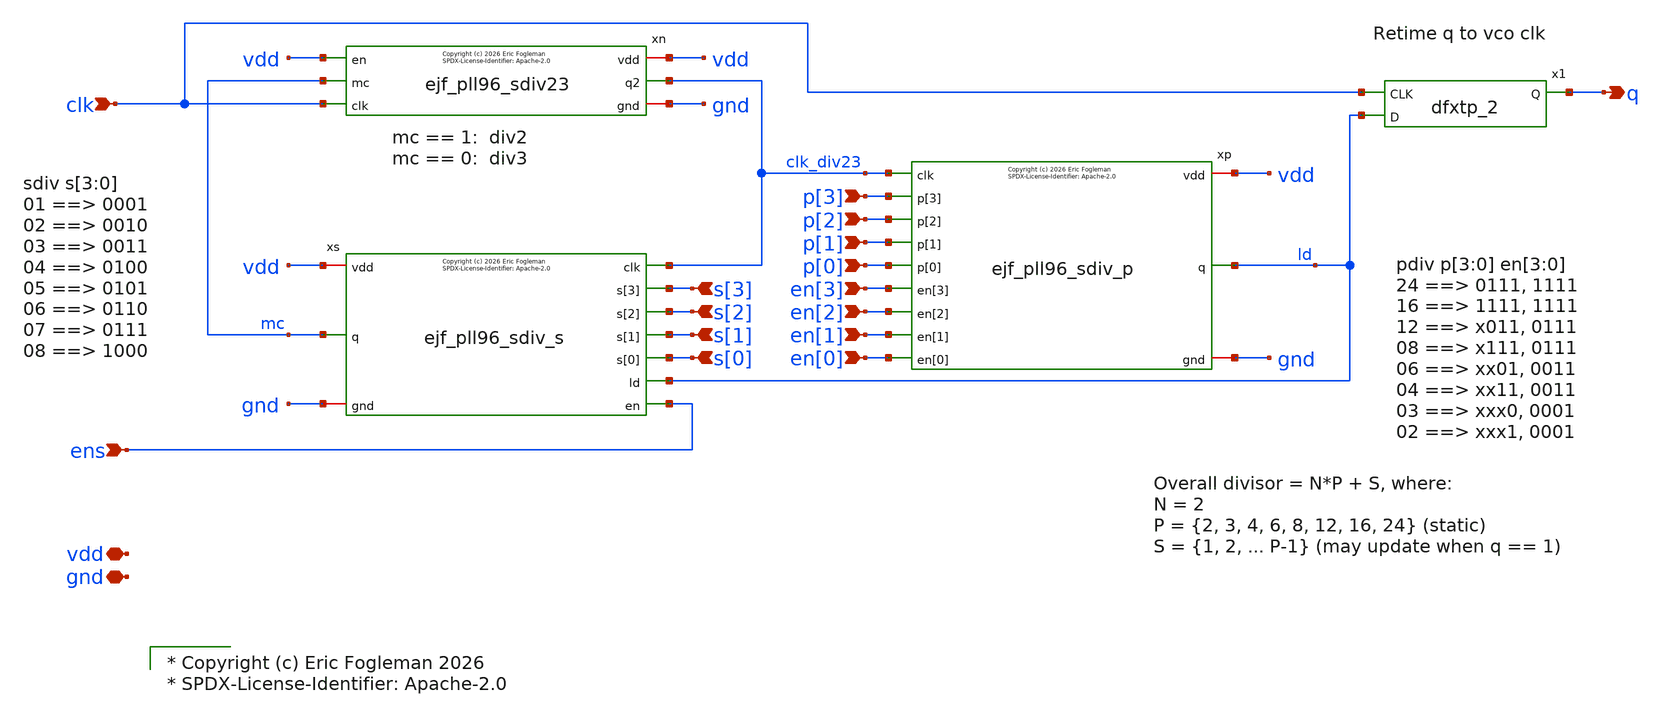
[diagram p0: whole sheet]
** sch_path: xschem/ejf_pll96_sdiv_mm.sch
* xschem/ejf_pll96_sdiv23.sym:
* Copyright (c) 2026 Eric Fogleman

* Copyright (c) Eric Fogleman 2026
* SPDX-License-Identifier: Apache-2.0

**.subckt ejf_pll96_sdiv_mm gnd clk q vdd p[3] p[2] p[1] p[0] en[3] en[2] en[1] s[0] s[1] s[2] s[3]
*+ ens en[0]
*.iopin gnd
*.ipin clk
*.opin q
*.iopin vdd
*.ipin p[3]
*.ipin p[2]
*.ipin p[1]
*.ipin p[0]
*.ipin en[3]
*.ipin en[2]
*.ipin en[1]
*.ipin s[0]
*.ipin s[1]
*.ipin s[2]
*.ipin s[3]
*.ipin ens
*.ipin en[0]
xn clk_div23 clk mc vdd gnd vdd ejf_pll96_sdiv23
xp clk_div23 p[0] en[1] p[1] ld en[2] p[2] en[3] p[3] vdd gnd en[0] ejf_pll96_sdiv_p
xs clk_div23 s[0] s[1] s[3] s[2] ld mc vdd gnd ens ejf_pll96_sdiv_s
x1 clk ld gnd gnd vdd vdd q sky130_fd_sc_ls__dfxtp_2
**.ends

* expanding   symbol:  ejf_pll96_sdiv23.sym # of pins=6
** sym_path: xschem/ejf_pll96_sdiv23.sym
** sch_path: xschem/ejf_pll96_sdiv23.sch
.subckt ejf_pll96_sdiv23 q2 clk mc vdd gnd en
*.ipin clk
*.ipin mc
*.opin q2
*.iopin vdd
*.iopin gnd
*.ipin en
x3 q1 mc q2_b gnd gnd vdd vdd d2 sky130_fd_sc_ls__o21a_1
**** begin user architecture code

* Copyright (c) Eric Fogleman 2026
* SPDX-License-Identifier: Apache-2.0

**** end user architecture code
x1 clk q2_b en gnd gnd vdd vdd q1 sky130_fd_sc_ls__edfxtp_1
x2 clk d2 en gnd gnd vdd vdd q2 q2_b sky130_fd_sc_ls__edfxbp_1
.ends


* expanding   symbol:  ejf_pll96_sdiv_p.sym # of pins=12
** sym_path: xschem/ejf_pll96_sdiv_p.sym
** sch_path: xschem/ejf_pll96_sdiv_p.sch
.subckt ejf_pll96_sdiv_p clk p[0] en[1] p[1] q en[2] p[2] en[3] p[3] vdd gnd en[0]
*.iopin vdd
*.iopin gnd
*.ipin clk
*.ipin p[1]
*.ipin p[2]
*.ipin p[3]
*.ipin en[3]
*.ipin en[2]
*.opin q
*.ipin en[1]
*.ipin p[0]
*.ipin en[0]
**** begin user architecture code

* Copyright (c) Eric Fogleman 2025
* SPDX-License-Identifier: Apache-2.0

**** end user architecture code
x5 q0 clk p[0] vdd gnd en[0] ejf_pll96_sdiv23
x8 q1 clk p[1] vdd gnd net2 ejf_pll96_sdiv23
x9 q0 en[1] gnd gnd vdd vdd net2 sky130_fd_sc_ls__and2_1
x10 q2 clk p[2] vdd gnd net3 ejf_pll96_sdiv23
x11 net2 q1 en[2] gnd gnd vdd vdd net3 sky130_fd_sc_ls__and3_1
x12 q3 clk p[3] vdd gnd net1 ejf_pll96_sdiv23
x7 net3 q2 en[3] gnd gnd vdd vdd net1 sky130_fd_sc_ls__and3_1
x1 q3 net4 gnd gnd vdd vdd q3_or_dis sky130_fd_sc_ls__or2_1
x2 en[3] gnd gnd vdd vdd net4 sky130_fd_sc_ls__inv_1
x3 q2 net5 gnd gnd vdd vdd q2_or_dis sky130_fd_sc_ls__or2_1
x13 en[2] gnd gnd vdd vdd net5 sky130_fd_sc_ls__inv_1
x14 q1 net6 gnd gnd vdd vdd q1_or_dis sky130_fd_sc_ls__or2_1
x15 en[1] gnd gnd vdd vdd net6 sky130_fd_sc_ls__inv_1
x16 q0 net7 gnd gnd vdd vdd q0_or_dis sky130_fd_sc_ls__or2_1
x17 en[0] gnd gnd vdd vdd net7 sky130_fd_sc_ls__inv_1
x18 q0_or_dis q1_or_dis q2_or_dis q3_or_dis gnd gnd vdd vdd q sky130_fd_sc_ls__and4_2
.ends


* expanding   symbol:  ejf_pll96_sdiv_s.sym # of pins=10
** sym_path: xschem/ejf_pll96_sdiv_s.sym
** sch_path: xschem/ejf_pll96_sdiv_s.sch
.subckt ejf_pll96_sdiv_s clk s[0] s[1] s[3] s[2] ld q vdd gnd en
*.ipin s[1]
*.ipin s[2]
*.ipin s[3]
*.ipin clk
*.opin q
*.ipin ld
*.ipin s[0]
*.ipin en
*.iopin vdd
*.iopin gnd
**** begin user architecture code

* Copyright (c) Eric Fogleman 2026
* SPDX-License-Identifier: Apache-2.0

**** end user architecture code
x3 q[3] q[2] q[1] q[0] gnd gnd vdd vdd tc sky130_fd_sc_ls__and4_2
x27 tc gnd gnd vdd vdd tc_b sky130_fd_sc_ls__inv_2
x2 clk net6 en[0] gnd gnd vdd vdd q[0] net1 sky130_fd_sc_ls__edfxbp_1
x1 net1 net10 ld_d2 gnd gnd vdd vdd net6 sky130_fd_sc_ls__mux2_1
x5 clk net7 en[1] gnd gnd vdd vdd q[1] net2 sky130_fd_sc_ls__edfxbp_1
x6 net2 net11 ld_d2 gnd gnd vdd vdd net7 sky130_fd_sc_ls__mux2_1
x8 clk net8 en[2] gnd gnd vdd vdd q[2] net3 sky130_fd_sc_ls__edfxbp_1
x9 net3 net12 ld_d2 gnd gnd vdd vdd net8 sky130_fd_sc_ls__mux2_1
x11 clk net9 net4 gnd gnd vdd vdd q[3] net5 sky130_fd_sc_ls__edfxbp_1
x12 net5 net13 ld_d2 gnd gnd vdd vdd net9 sky130_fd_sc_ls__mux2_1
x4 tc_b ld_d2 gnd gnd vdd vdd en[0] sky130_fd_sc_ls__or2_1
x16 s[0] gnd gnd vdd vdd net10 sky130_fd_sc_ls__inv_1
x20 en[0] q[0] ld_d2 gnd gnd vdd vdd en[1] sky130_fd_sc_ls__a21o_1
x7 en[1] q[1] ld_d2 gnd gnd vdd vdd en[2] sky130_fd_sc_ls__a21o_1
x10 en[2] q[2] ld_d2 gnd gnd vdd vdd net4 sky130_fd_sc_ls__a21o_1
x13 ld gnd gnd vdd vdd ld_d2 sky130_fd_sc_ls__buf_2
x17 s[1] gnd gnd vdd vdd net11 sky130_fd_sc_ls__inv_1
x18 s[2] gnd gnd vdd vdd net12 sky130_fd_sc_ls__inv_1
x19 s[3] gnd gnd vdd vdd net13 sky130_fd_sc_ls__inv_1
x14 tc_b en gnd gnd vdd vdd q sky130_fd_sc_ls__nand2_2
.ends

.end
